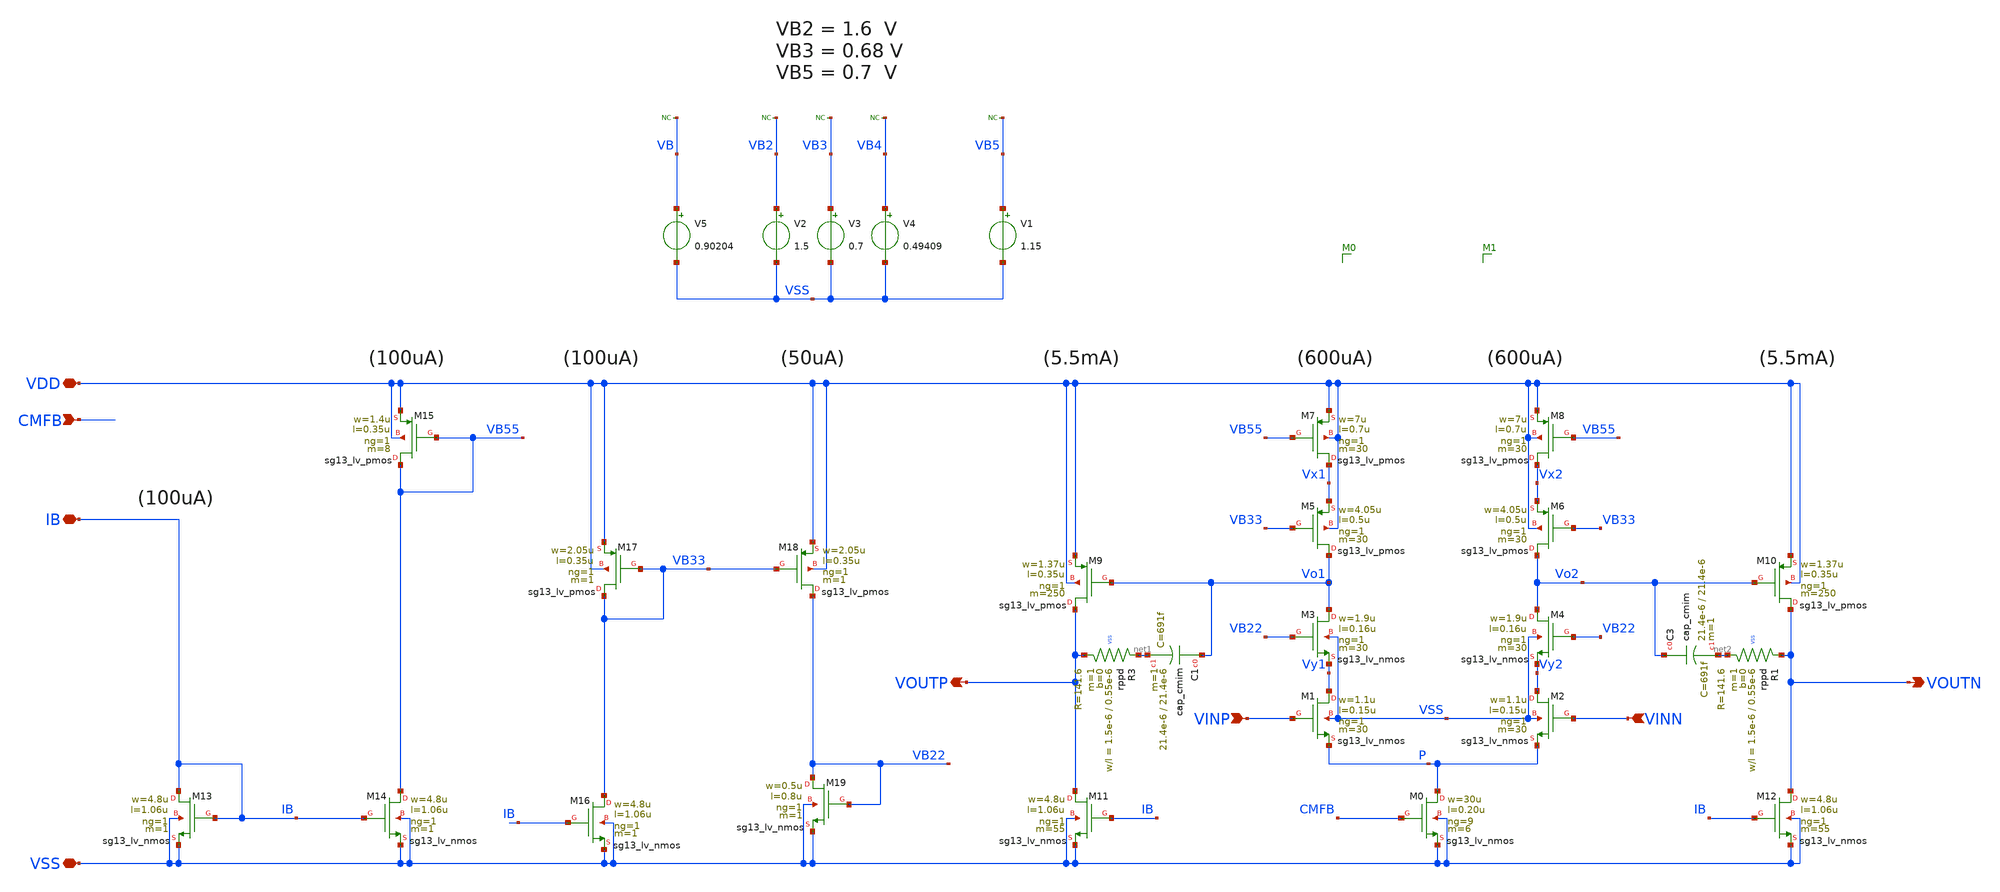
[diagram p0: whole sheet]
** sch_path: OTA_Telescopic_backup/OTA_Telescopic_v1/OTA_Telescopic_core.sch
**.subckt OTA_Telescopic_core VDD VSS VINP VINN VOUTN VOUTP CMFB IB
*.iopin VDD
*.iopin VSS
*.ipin VINP
*.ipin VINN
*.opin VOUTN
*.opin VOUTP
*.ipin CMFB
*.iopin IB
V2 VB2 VSS 1.5
V3 VB3 VSS 0.7
V4 VB4 VSS 0.49409
V1 VB5 VSS 1.15
* noconn VB2
* noconn VB3
* noconn VB4
* noconn VB5
V5 VB VSS 0.90204
* noconn VB
XM15 VB55 VB55 VDD VDD sg13_lv_pmos w=1.4u l=0.35u ng=1 m=8 mm_ok=1
XM17 VB33 VB33 VDD VDD sg13_lv_pmos w=2.05u l=0.35u ng=1 m=1 mm_ok=1
XM18 VB22 VB33 VDD VDD sg13_lv_pmos w=2.05u l=0.35u ng=1 m=1 mm_ok=1
XM9 VOUTP Vo1 VDD VDD sg13_lv_pmos w=1.37u l=0.35u ng=1 m=250 mm_ok=1
XM7 Vx1 VB55 VDD VDD sg13_lv_pmos w=7u l=0.7u ng=1 m=30 mm_ok=1
XM5 Vo1 VB33 Vx1 VDD sg13_lv_pmos w=4.05u l=0.5u ng=1 m=30 mm_ok=1
XM8 Vx2 VB55 VDD VDD sg13_lv_pmos w=7u l=0.7u ng=1 m=30 mm_ok=1
XM6 Vo2 VB33 Vx2 VDD sg13_lv_pmos w=4.05u l=0.5u ng=1 m=30 mm_ok=1
XM10 VOUTN Vo2 VDD VDD sg13_lv_pmos w=1.37u l=0.35u ng=1 m=250 mm_ok=1
XM13 IB IB VSS VSS sg13_lv_nmos w=4.8u l=1.06u ng=1 m=1 mm_ok=1
XM14 VB55 IB VSS VSS sg13_lv_nmos w=4.8u l=1.06u ng=1 m=1 mm_ok=1
XM16 VB33 IB VSS VSS sg13_lv_nmos w=4.8u l=1.06u ng=1 m=1 mm_ok=1
XM19 VB22 VB22 VSS VSS sg13_lv_nmos w=0.5u l=0.8u ng=1 m=1 mm_ok=1
XM11 VOUTP IB VSS VSS sg13_lv_nmos w=4.8u l=1.06u ng=1 m=55 mm_ok=1
XM0 P CMFB VSS VSS sg13_lv_nmos w=30u l=0.20u ng=9 m=6 mm_ok=1
XM3 Vo1 VB22 Vy1 VSS sg13_lv_nmos w=1.9u l=0.16u ng=1 m=30 mm_ok=1
XM1 Vy1 VINP P VSS sg13_lv_nmos w=1.1u l=0.15u ng=1 m=30 mm_ok=1
XM4 Vo2 VB22 Vy2 VSS sg13_lv_nmos w=1.9u l=0.16u ng=1 m=30 mm_ok=1
XM2 Vy2 VINN P VSS sg13_lv_nmos w=1.1u l=0.15u ng=1 m=30 mm_ok=1
XM12 VOUTN IB VSS VSS sg13_lv_nmos w=4.8u l=1.06u ng=1 m=55 mm_ok=1
XR3 net1 VOUTP VSS rppd w=1.5e-6 l=0.55e-6 m=1 b=0 mm_ok=1
XR1 VOUTN net2 VSS rppd w=1.5e-6 l=0.55e-6 m=1 b=0 mm_ok=1
XC3 Vo2 net2 cap_cmim w=21.4e-6 l=21.4e-6 m=1 mm_ok=1
XC1 Vo1 net1 cap_cmim w=21.4e-6 l=21.4e-6 m=1 mm_ok=1
**.ends
.end
